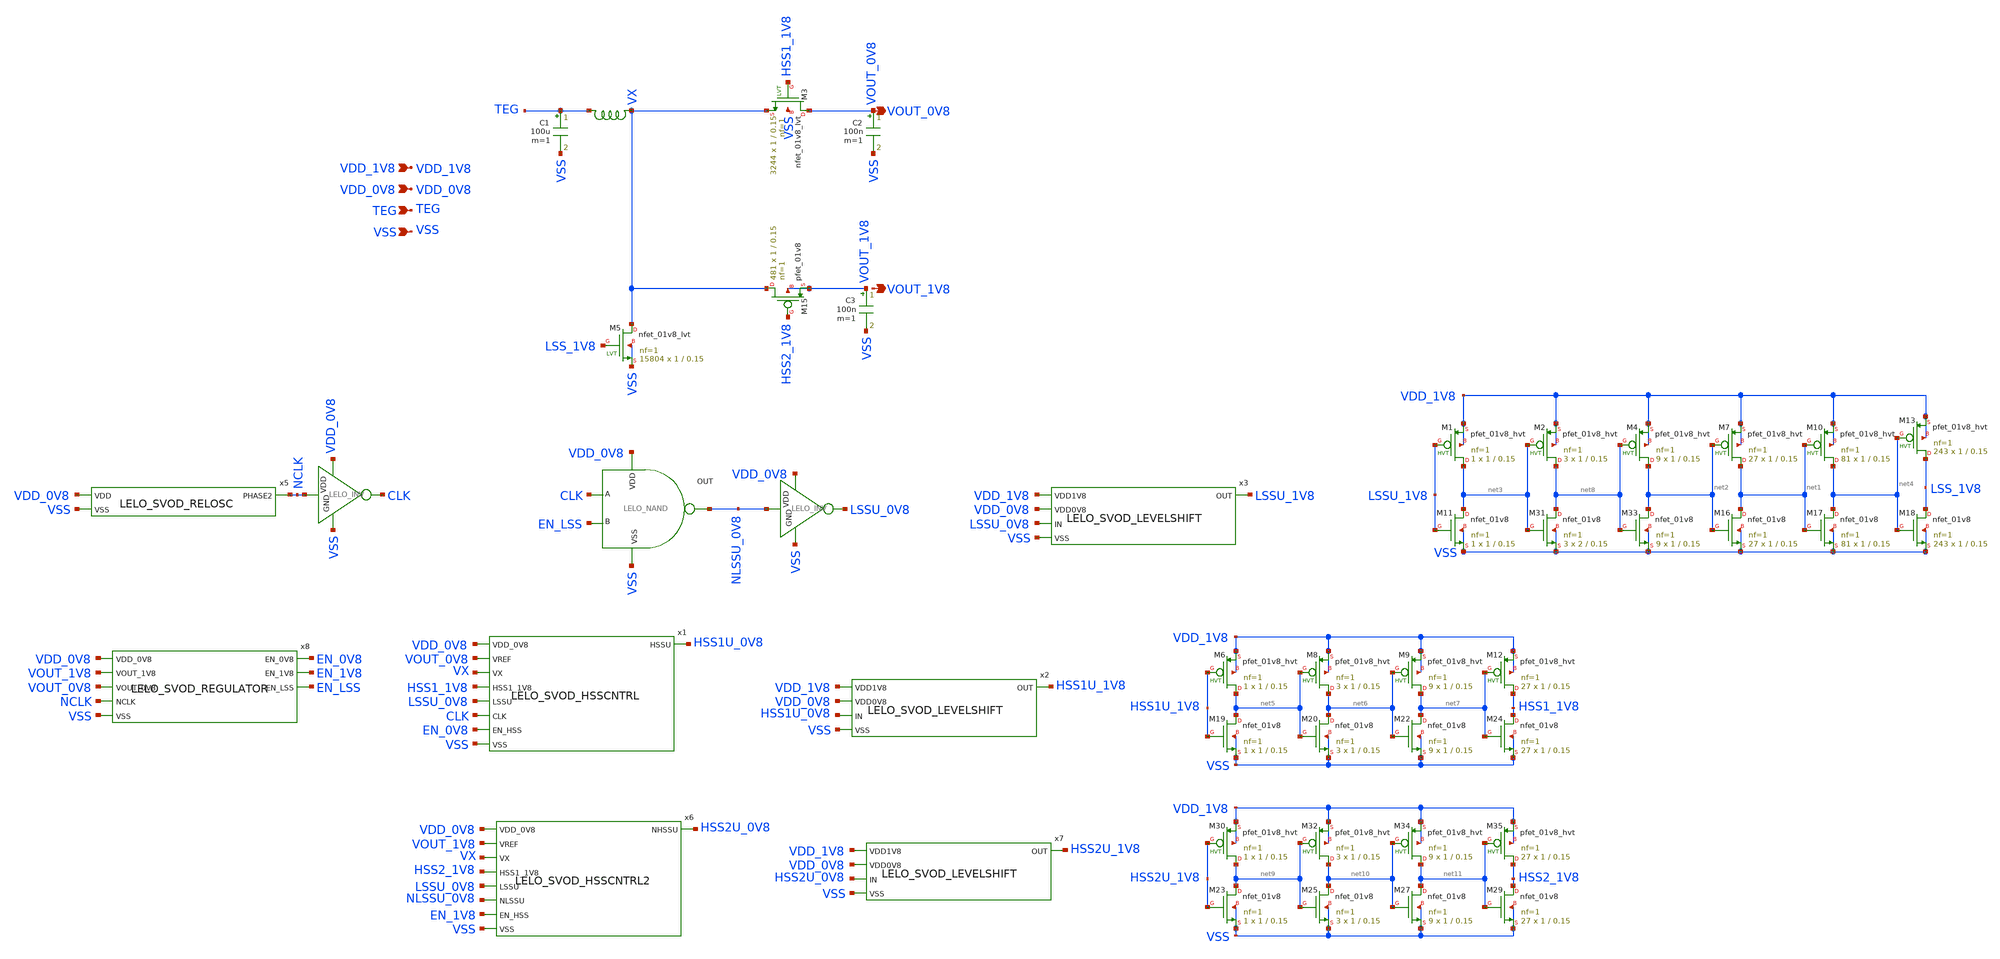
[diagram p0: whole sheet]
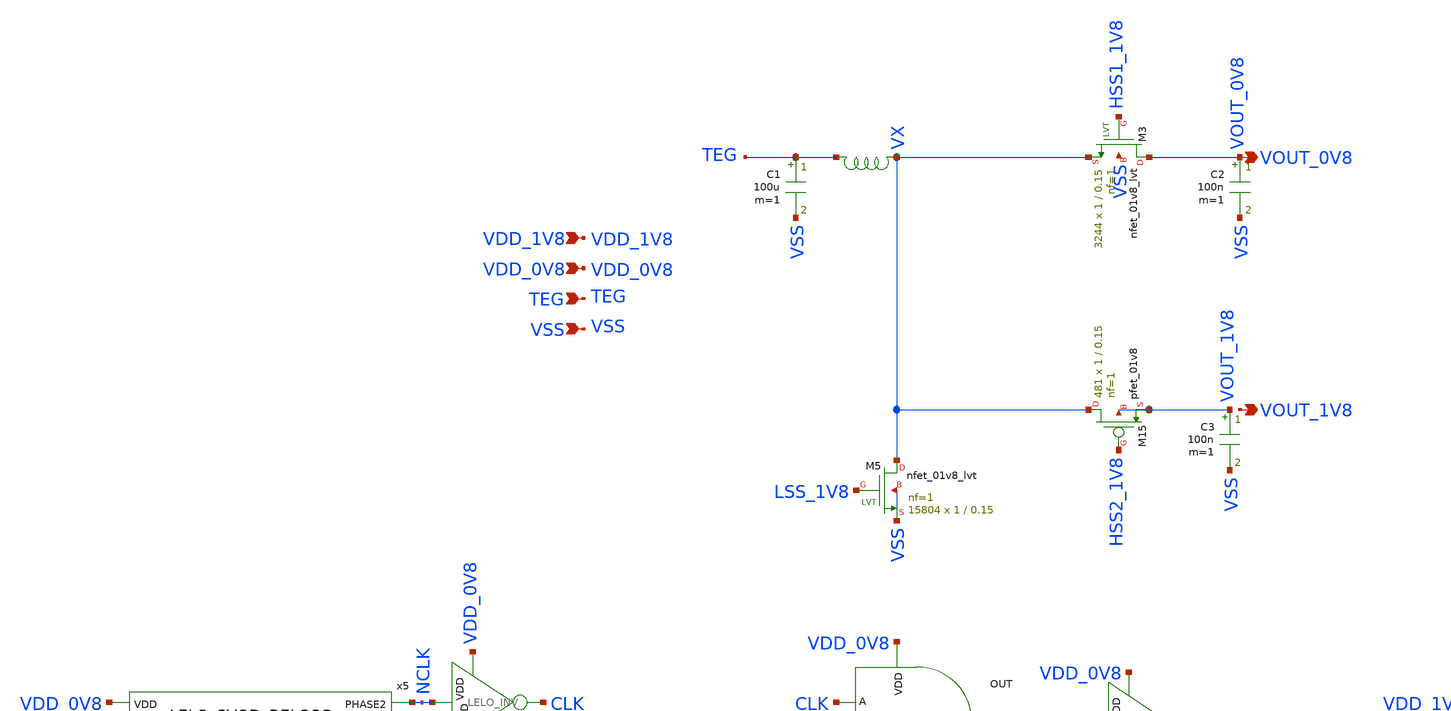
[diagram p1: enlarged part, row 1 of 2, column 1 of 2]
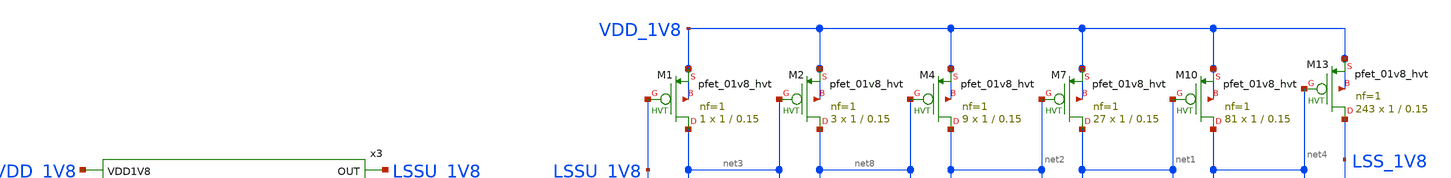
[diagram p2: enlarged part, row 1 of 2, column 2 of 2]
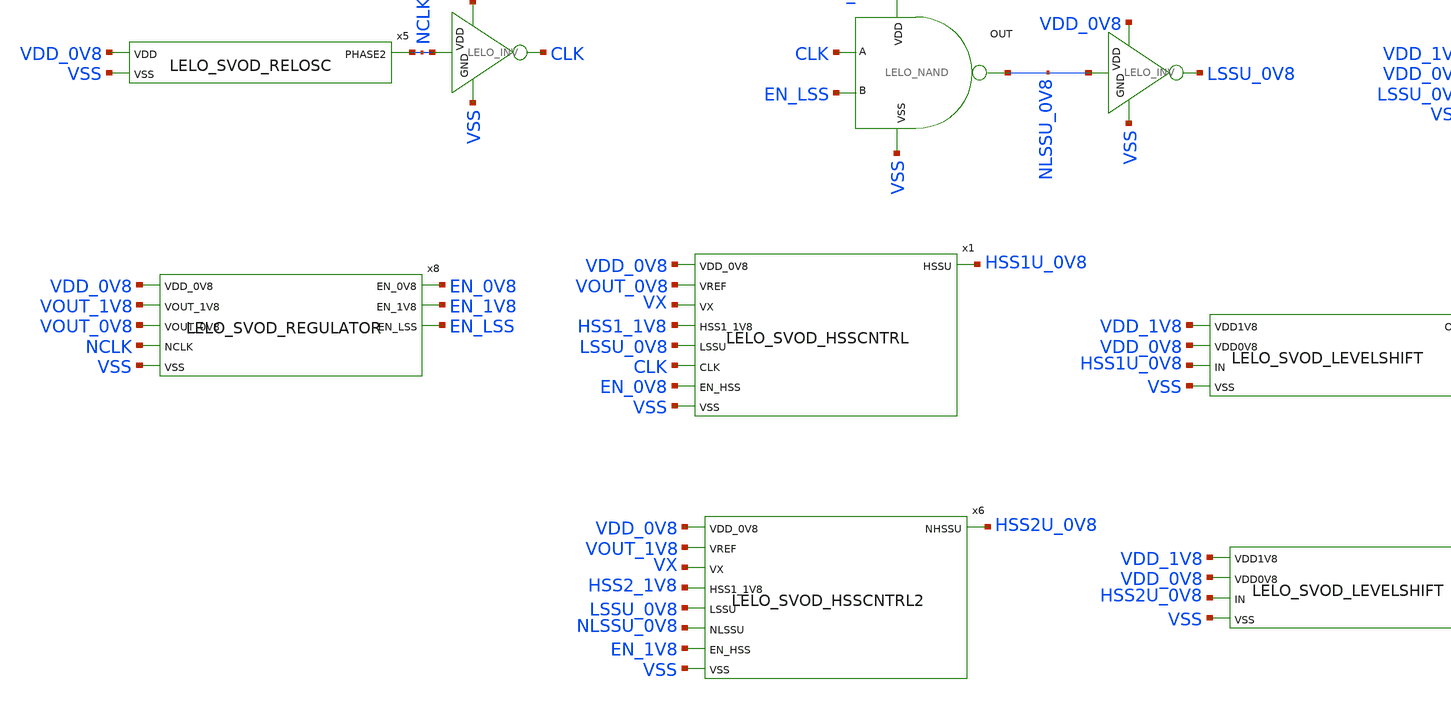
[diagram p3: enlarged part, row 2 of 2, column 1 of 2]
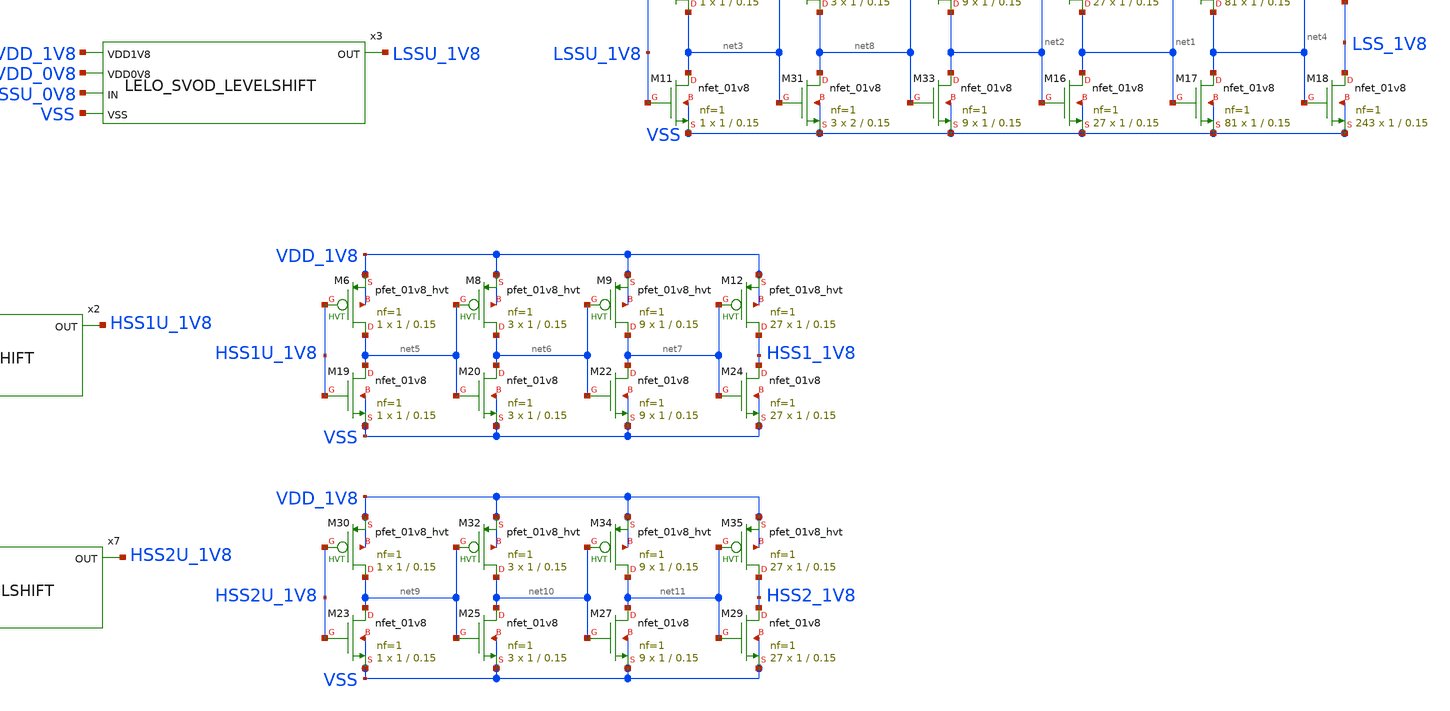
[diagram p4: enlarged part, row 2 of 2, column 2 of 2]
** sch_path: design/LELO_SVOD_SKY130A/LELO_SVOD_BOOST_2.sch
**.subckt LELO_SVOD_BOOST_2 VSS TEG VDD_0V8 VDD_1V8 VOUT_0V8 VOUT_1V8
*.ipin VSS
*.ipin TEG
*.ipin VDD_0V8
*.ipin VDD_1V8
*.opin VOUT_0V8
*.opin VOUT_1V8
C1 TEG VSS 100u m=1
XM5 VX LSS_1V8 VSS VSS sky130_fd_pr__nfet_01v8_lvt L=0.15 W=1 nf=1 ad='int((1 + 1)/2) * 1 / 1 * 0.29'
+ as='int((1 + 2)/2) * 1 / 1 * 0.29' pd='2*int((1 + 1)/2) * (1 / 1 + 0.29)' ps='2*int((1 + 2)/2) * (1 / 1 + 0.29)'
+ nrd='0.29 / 1 ' nrs='0.29 / 1 ' sa=0 sb=0 sd=0 mult=15804 m=15804
C2 VOUT_0V8 VSS 100n m=1
XM11 net3 LSSU_1V8 VSS VSS sky130_fd_pr__nfet_01v8 L=0.15 W=1 nf=1 ad='int((1 + 1)/2) * 1 / 1 * 0.29'
+ as='int((1 + 2)/2) * 1 / 1 * 0.29' pd='2*int((1 + 1)/2) * (1 / 1 + 0.29)' ps='2*int((1 + 2)/2) * (1 / 1 + 0.29)'
+ nrd='0.29 / 1 ' nrs='0.29 / 1 ' sa=0 sb=0 sd=0 mult=1 m=1
XM16 net1 net2 VSS VSS sky130_fd_pr__nfet_01v8 L=0.15 W=1 nf=1 ad='int((1 + 1)/2) * 1 / 1 * 0.29' as='int((1 + 2)/2) * 1 / 1 * 0.29'
+ pd='2*int((1 + 1)/2) * (1 / 1 + 0.29)' ps='2*int((1 + 2)/2) * (1 / 1 + 0.29)' nrd='0.29 / 1 ' nrs='0.29 / 1 '
+ sa=0 sb=0 sd=0 mult=27 m=27
XM17 net4 net1 VSS VSS sky130_fd_pr__nfet_01v8 L=0.15 W=1 nf=1 ad='int((1 + 1)/2) * 1 / 1 * 0.29' as='int((1 + 2)/2) * 1 / 1 * 0.29'
+ pd='2*int((1 + 1)/2) * (1 / 1 + 0.29)' ps='2*int((1 + 2)/2) * (1 / 1 + 0.29)' nrd='0.29 / 1 ' nrs='0.29 / 1 '
+ sa=0 sb=0 sd=0 mult=81 m=81
XM18 LSS_1V8 net4 VSS VSS sky130_fd_pr__nfet_01v8 L=0.15 W=1 nf=1 ad='int((1 + 1)/2) * 1 / 1 * 0.29'
+ as='int((1 + 2)/2) * 1 / 1 * 0.29' pd='2*int((1 + 1)/2) * (1 / 1 + 0.29)' ps='2*int((1 + 2)/2) * (1 / 1 + 0.29)'
+ nrd='0.29 / 1 ' nrs='0.29 / 1 ' sa=0 sb=0 sd=0 mult=243 m=243
XM19 net5 HSS1U_1V8 VSS VSS sky130_fd_pr__nfet_01v8 L=0.15 W=1 nf=1 ad='int((1 + 1)/2) * 1 / 1 * 0.29'
+ as='int((1 + 2)/2) * 1 / 1 * 0.29' pd='2*int((1 + 1)/2) * (1 / 1 + 0.29)' ps='2*int((1 + 2)/2) * (1 / 1 + 0.29)'
+ nrd='0.29 / 1 ' nrs='0.29 / 1 ' sa=0 sb=0 sd=0 mult=1 m=1
XM20 net6 net5 VSS VSS sky130_fd_pr__nfet_01v8 L=0.15 W=1 nf=1 ad='int((1 + 1)/2) * 1 / 1 * 0.29' as='int((1 + 2)/2) * 1 / 1 * 0.29'
+ pd='2*int((1 + 1)/2) * (1 / 1 + 0.29)' ps='2*int((1 + 2)/2) * (1 / 1 + 0.29)' nrd='0.29 / 1 ' nrs='0.29 / 1 '
+ sa=0 sb=0 sd=0 mult=3 m=3
XM22 net7 net6 VSS VSS sky130_fd_pr__nfet_01v8 L=0.15 W=1 nf=1 ad='int((1 + 1)/2) * 1 / 1 * 0.29' as='int((1 + 2)/2) * 1 / 1 * 0.29'
+ pd='2*int((1 + 1)/2) * (1 / 1 + 0.29)' ps='2*int((1 + 2)/2) * (1 / 1 + 0.29)' nrd='0.29 / 1 ' nrs='0.29 / 1 '
+ sa=0 sb=0 sd=0 mult=9 m=9
XM24 HSS1_1V8 net7 VSS VSS sky130_fd_pr__nfet_01v8 L=0.15 W=1 nf=1 ad='int((1 + 1)/2) * 1 / 1 * 0.29'
+ as='int((1 + 2)/2) * 1 / 1 * 0.29' pd='2*int((1 + 1)/2) * (1 / 1 + 0.29)' ps='2*int((1 + 2)/2) * (1 / 1 + 0.29)'
+ nrd='0.29 / 1 ' nrs='0.29 / 1 ' sa=0 sb=0 sd=0 mult=27 m=27
XM31 net8 net3 VSS VSS sky130_fd_pr__nfet_01v8 L=0.15 W=2 nf=1 ad='int((1 + 1)/2) * 2 / 1 * 0.29' as='int((1 + 2)/2) * 2 / 1 * 0.29'
+ pd='2*int((1 + 1)/2) * (2 / 1 + 0.29)' ps='2*int((1 + 2)/2) * (2 / 1 + 0.29)' nrd='0.29 / 2 ' nrs='0.29 / 2 '
+ sa=0 sb=0 sd=0 mult=3 m=3
XM33 net2 net8 VSS VSS sky130_fd_pr__nfet_01v8 L=0.15 W=1 nf=1 ad='int((1 + 1)/2) * 1 / 1 * 0.29' as='int((1 + 2)/2) * 1 / 1 * 0.29'
+ pd='2*int((1 + 1)/2) * (1 / 1 + 0.29)' ps='2*int((1 + 2)/2) * (1 / 1 + 0.29)' nrd='0.29 / 1 ' nrs='0.29 / 1 '
+ sa=0 sb=0 sd=0 mult=9 m=9
XM3 VOUT_0V8 HSS1_1V8 VX VSS sky130_fd_pr__nfet_01v8_lvt L=0.15 W=1 nf=1 ad='int((1 + 1)/2) * 1 / 1 * 0.29'
+ as='int((1 + 2)/2) * 1 / 1 * 0.29' pd='2*int((1 + 1)/2) * (1 / 1 + 0.29)' ps='2*int((1 + 2)/2) * (1 / 1 + 0.29)'
+ nrd='0.29 / 1 ' nrs='0.29 / 1 ' sa=0 sb=0 sd=0 mult=3244 m=3244
x1 VDD_0V8 VOUT_0V8 HSS1U_0V8 VX HSS1_1V8 LSSU_0V8 CLK EN_0V8 VSS LELO_SVOD_HSSCNTRL
x2 VDD_1V8 HSS1U_1V8 VDD_0V8 HSS1U_0V8 VSS LELO_SVOD_LEVELSHIFT
x3 VDD_1V8 LSSU_1V8 VDD_0V8 LSSU_0V8 VSS LELO_SVOD_LEVELSHIFT
XM6 net5 HSS1U_1V8 VDD_1V8 VDD_1V8 sky130_fd_pr__pfet_01v8_hvt L=0.15 W=1 nf=1 ad='int((1 + 1)/2) * 1 / 1 * 0.29'
+ as='int((1 + 2)/2) * 1 / 1 * 0.29' pd='2*int((1 + 1)/2) * (1 / 1 + 0.29)' ps='2*int((1 + 2)/2) * (1 / 1 + 0.29)'
+ nrd='0.29 / 1 ' nrs='0.29 / 1 ' sa=0 sb=0 sd=0 mult=1 m=1
XM8 net6 net5 VDD_1V8 VDD_1V8 sky130_fd_pr__pfet_01v8_hvt L=0.15 W=1 nf=1 ad='int((1 + 1)/2) * 1 / 1 * 0.29'
+ as='int((1 + 2)/2) * 1 / 1 * 0.29' pd='2*int((1 + 1)/2) * (1 / 1 + 0.29)' ps='2*int((1 + 2)/2) * (1 / 1 + 0.29)'
+ nrd='0.29 / 1 ' nrs='0.29 / 1 ' sa=0 sb=0 sd=0 mult=3 m=3
XM9 net7 net6 VDD_1V8 VDD_1V8 sky130_fd_pr__pfet_01v8_hvt L=0.15 W=1 nf=1 ad='int((1 + 1)/2) * 1 / 1 * 0.29'
+ as='int((1 + 2)/2) * 1 / 1 * 0.29' pd='2*int((1 + 1)/2) * (1 / 1 + 0.29)' ps='2*int((1 + 2)/2) * (1 / 1 + 0.29)'
+ nrd='0.29 / 1 ' nrs='0.29 / 1 ' sa=0 sb=0 sd=0 mult=9 m=9
XM12 HSS1_1V8 net7 VDD_1V8 VDD_1V8 sky130_fd_pr__pfet_01v8_hvt L=0.15 W=1 nf=1 ad='int((1 + 1)/2) * 1 / 1 * 0.29'
+ as='int((1 + 2)/2) * 1 / 1 * 0.29' pd='2*int((1 + 1)/2) * (1 / 1 + 0.29)' ps='2*int((1 + 2)/2) * (1 / 1 + 0.29)'
+ nrd='0.29 / 1 ' nrs='0.29 / 1 ' sa=0 sb=0 sd=0 mult=27 m=27
XM1 net3 LSSU_1V8 VDD_1V8 VDD_1V8 sky130_fd_pr__pfet_01v8_hvt L=0.15 W=1 nf=1 ad='int((1 + 1)/2) * 1 / 1 * 0.29'
+ as='int((1 + 2)/2) * 1 / 1 * 0.29' pd='2*int((1 + 1)/2) * (1 / 1 + 0.29)' ps='2*int((1 + 2)/2) * (1 / 1 + 0.29)'
+ nrd='0.29 / 1 ' nrs='0.29 / 1 ' sa=0 sb=0 sd=0 mult=1 m=1
XM2 net8 net3 VDD_1V8 VDD_1V8 sky130_fd_pr__pfet_01v8_hvt L=0.15 W=1 nf=1 ad='int((1 + 1)/2) * 1 / 1 * 0.29'
+ as='int((1 + 2)/2) * 1 / 1 * 0.29' pd='2*int((1 + 1)/2) * (1 / 1 + 0.29)' ps='2*int((1 + 2)/2) * (1 / 1 + 0.29)'
+ nrd='0.29 / 1 ' nrs='0.29 / 1 ' sa=0 sb=0 sd=0 mult=3 m=3
XM4 net2 net8 VDD_1V8 VDD_1V8 sky130_fd_pr__pfet_01v8_hvt L=0.15 W=1 nf=1 ad='int((1 + 1)/2) * 1 / 1 * 0.29'
+ as='int((1 + 2)/2) * 1 / 1 * 0.29' pd='2*int((1 + 1)/2) * (1 / 1 + 0.29)' ps='2*int((1 + 2)/2) * (1 / 1 + 0.29)'
+ nrd='0.29 / 1 ' nrs='0.29 / 1 ' sa=0 sb=0 sd=0 mult=9 m=9
XM7 net1 net2 VDD_1V8 VDD_1V8 sky130_fd_pr__pfet_01v8_hvt L=0.15 W=1 nf=1 ad='int((1 + 1)/2) * 1 / 1 * 0.29'
+ as='int((1 + 2)/2) * 1 / 1 * 0.29' pd='2*int((1 + 1)/2) * (1 / 1 + 0.29)' ps='2*int((1 + 2)/2) * (1 / 1 + 0.29)'
+ nrd='0.29 / 1 ' nrs='0.29 / 1 ' sa=0 sb=0 sd=0 mult=27 m=27
XM10 net4 net1 VDD_1V8 VDD_1V8 sky130_fd_pr__pfet_01v8_hvt L=0.15 W=1 nf=1 ad='int((1 + 1)/2) * 1 / 1 * 0.29'
+ as='int((1 + 2)/2) * 1 / 1 * 0.29' pd='2*int((1 + 1)/2) * (1 / 1 + 0.29)' ps='2*int((1 + 2)/2) * (1 / 1 + 0.29)'
+ nrd='0.29 / 1 ' nrs='0.29 / 1 ' sa=0 sb=0 sd=0 mult=81 m=81
XM13 LSS_1V8 net4 VDD_1V8 VDD_1V8 sky130_fd_pr__pfet_01v8_hvt L=0.15 W=1 nf=1 ad='int((1 + 1)/2) * 1 / 1 * 0.29'
+ as='int((1 + 2)/2) * 1 / 1 * 0.29' pd='2*int((1 + 1)/2) * (1 / 1 + 0.29)' ps='2*int((1 + 2)/2) * (1 / 1 + 0.29)'
+ nrd='0.29 / 1 ' nrs='0.29 / 1 ' sa=0 sb=0 sd=0 mult=243 m=243
x4 VX TEG XGL6030-183_sat
x5 VDD_0V8 VSS NCLK LELO_SVOD_RELOSC
XM15 VX HSS2_1V8 VOUT_1V8 VOUT_1V8 sky130_fd_pr__pfet_01v8 L=0.15 W=1 nf=1 ad='int((1 + 1)/2) * 1 / 1 * 0.29'
+ as='int((1 + 2)/2) * 1 / 1 * 0.29' pd='2*int((1 + 1)/2) * (1 / 1 + 0.29)' ps='2*int((1 + 2)/2) * (1 / 1 + 0.29)'
+ nrd='0.29 / 1 ' nrs='0.29 / 1 ' sa=0 sb=0 sd=0 mult=481 m=481
C3 VOUT_1V8 VSS 100n m=1
x6 VDD_0V8 VOUT_1V8 HSS2U_0V8 VX HSS2_1V8 LSSU_0V8 NLSSU_0V8 EN_1V8 VSS LELO_SVOD_HSSCNTRL2
x7 VDD_1V8 HSS2U_1V8 VDD_0V8 HSS2U_0V8 VSS LELO_SVOD_LEVELSHIFT
XM23 net9 HSS2U_1V8 VSS VSS sky130_fd_pr__nfet_01v8 L=0.15 W=1 nf=1 ad='int((1 + 1)/2) * 1 / 1 * 0.29'
+ as='int((1 + 2)/2) * 1 / 1 * 0.29' pd='2*int((1 + 1)/2) * (1 / 1 + 0.29)' ps='2*int((1 + 2)/2) * (1 / 1 + 0.29)'
+ nrd='0.29 / 1 ' nrs='0.29 / 1 ' sa=0 sb=0 sd=0 mult=1 m=1
XM25 net10 net9 VSS VSS sky130_fd_pr__nfet_01v8 L=0.15 W=1 nf=1 ad='int((1 + 1)/2) * 1 / 1 * 0.29' as='int((1 + 2)/2) * 1 / 1 * 0.29'
+ pd='2*int((1 + 1)/2) * (1 / 1 + 0.29)' ps='2*int((1 + 2)/2) * (1 / 1 + 0.29)' nrd='0.29 / 1 ' nrs='0.29 / 1 '
+ sa=0 sb=0 sd=0 mult=3 m=3
XM27 net11 net10 VSS VSS sky130_fd_pr__nfet_01v8 L=0.15 W=1 nf=1 ad='int((1 + 1)/2) * 1 / 1 * 0.29' as='int((1 + 2)/2) * 1 / 1 * 0.29'
+ pd='2*int((1 + 1)/2) * (1 / 1 + 0.29)' ps='2*int((1 + 2)/2) * (1 / 1 + 0.29)' nrd='0.29 / 1 ' nrs='0.29 / 1 '
+ sa=0 sb=0 sd=0 mult=9 m=9
XM29 HSS2_1V8 net11 VSS VSS sky130_fd_pr__nfet_01v8 L=0.15 W=1 nf=1 ad='int((1 + 1)/2) * 1 / 1 * 0.29'
+ as='int((1 + 2)/2) * 1 / 1 * 0.29' pd='2*int((1 + 1)/2) * (1 / 1 + 0.29)' ps='2*int((1 + 2)/2) * (1 / 1 + 0.29)'
+ nrd='0.29 / 1 ' nrs='0.29 / 1 ' sa=0 sb=0 sd=0 mult=27 m=27
XM30 net9 HSS2U_1V8 VDD_1V8 VDD_1V8 sky130_fd_pr__pfet_01v8_hvt L=0.15 W=1 nf=1 ad='int((1 + 1)/2) * 1 / 1 * 0.29'
+ as='int((1 + 2)/2) * 1 / 1 * 0.29' pd='2*int((1 + 1)/2) * (1 / 1 + 0.29)' ps='2*int((1 + 2)/2) * (1 / 1 + 0.29)'
+ nrd='0.29 / 1 ' nrs='0.29 / 1 ' sa=0 sb=0 sd=0 mult=1 m=1
XM32 net10 net9 VDD_1V8 VDD_1V8 sky130_fd_pr__pfet_01v8_hvt L=0.15 W=1 nf=1 ad='int((1 + 1)/2) * 1 / 1 * 0.29'
+ as='int((1 + 2)/2) * 1 / 1 * 0.29' pd='2*int((1 + 1)/2) * (1 / 1 + 0.29)' ps='2*int((1 + 2)/2) * (1 / 1 + 0.29)'
+ nrd='0.29 / 1 ' nrs='0.29 / 1 ' sa=0 sb=0 sd=0 mult=3 m=3
XM34 net11 net10 VDD_1V8 VDD_1V8 sky130_fd_pr__pfet_01v8_hvt L=0.15 W=1 nf=1 ad='int((1 + 1)/2) * 1 / 1 * 0.29'
+ as='int((1 + 2)/2) * 1 / 1 * 0.29' pd='2*int((1 + 1)/2) * (1 / 1 + 0.29)' ps='2*int((1 + 2)/2) * (1 / 1 + 0.29)'
+ nrd='0.29 / 1 ' nrs='0.29 / 1 ' sa=0 sb=0 sd=0 mult=9 m=9
XM35 HSS2_1V8 net11 VDD_1V8 VDD_1V8 sky130_fd_pr__pfet_01v8_hvt L=0.15 W=1 nf=1 ad='int((1 + 1)/2) * 1 / 1 * 0.29'
+ as='int((1 + 2)/2) * 1 / 1 * 0.29' pd='2*int((1 + 1)/2) * (1 / 1 + 0.29)' ps='2*int((1 + 2)/2) * (1 / 1 + 0.29)'
+ nrd='0.29 / 1 ' nrs='0.29 / 1 ' sa=0 sb=0 sd=0 mult=27 m=27
x8 EN_0V8 EN_1V8 EN_LSS VDD_0V8 VOUT_1V8 VOUT_0V8 NCLK VSS LELO_SVOD_REGULATOR
x9 VDD_0V8 NLSSU_0V8 CLK EN_LSS VSS LELO_NAND
x10 VDD_0V8 NLSSU_0V8 LSSU_0V8 VSS LELO_INV
x11 VDD_0V8 NCLK CLK VSS LELO_INV
**.ends
.end
